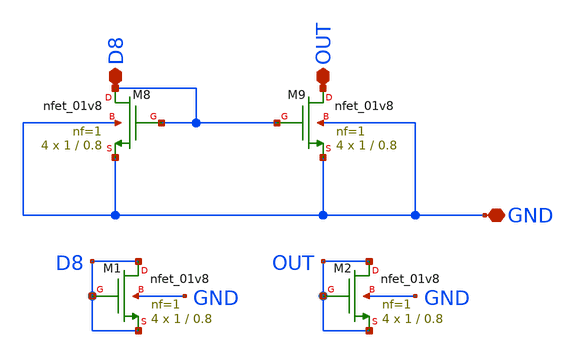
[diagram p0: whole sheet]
** sch_path: NMOS89/NMOS89.sch
**.subckt NMOS89 GND OUT D8
*.iopin GND
*.iopin OUT
*.iopin D8
XM8 D8 D8 GND GND sky130_fd_pr__nfet_01v8 L=0.8 W=1 nf=1 ad='int((nf+1)/2) * W/nf * 0.29' as='int((nf+2)/2) * W/nf * 0.29'
+ pd='2*int((nf+1)/2) * (W/nf + 0.29)' ps='2*int((nf+2)/2) * (W/nf + 0.29)' nrd='0.29 / W' nrs='0.29 / W'
+ sa=0 sb=0 sd=0 mult=4 m=4
XM9 OUT D8 GND GND sky130_fd_pr__nfet_01v8 L=0.8 W=1 nf=1 ad='int((nf+1)/2) * W/nf * 0.29' as='int((nf+2)/2) * W/nf * 0.29'
+ pd='2*int((nf+1)/2) * (W/nf + 0.29)' ps='2*int((nf+2)/2) * (W/nf + 0.29)' nrd='0.29 / W' nrs='0.29 / W'
+ sa=0 sb=0 sd=0 mult=4 m=4
XM1 D8 D8 D8 GND sky130_fd_pr__nfet_01v8 L=0.8 W=1 nf=1 ad='int((nf+1)/2) * W/nf * 0.29' as='int((nf+2)/2) * W/nf * 0.29'
+ pd='2*int((nf+1)/2) * (W/nf + 0.29)' ps='2*int((nf+2)/2) * (W/nf + 0.29)' nrd='0.29 / W' nrs='0.29 / W'
+ sa=0 sb=0 sd=0 mult=4 m=4
XM2 OUT OUT OUT GND sky130_fd_pr__nfet_01v8 L=0.8 W=1 nf=1 ad='int((nf+1)/2) * W/nf * 0.29' as='int((nf+2)/2) * W/nf * 0.29'
+ pd='2*int((nf+1)/2) * (W/nf + 0.29)' ps='2*int((nf+2)/2) * (W/nf + 0.29)' nrd='0.29 / W' nrs='0.29 / W'
+ sa=0 sb=0 sd=0 mult=4 m=4
**.ends
.end
